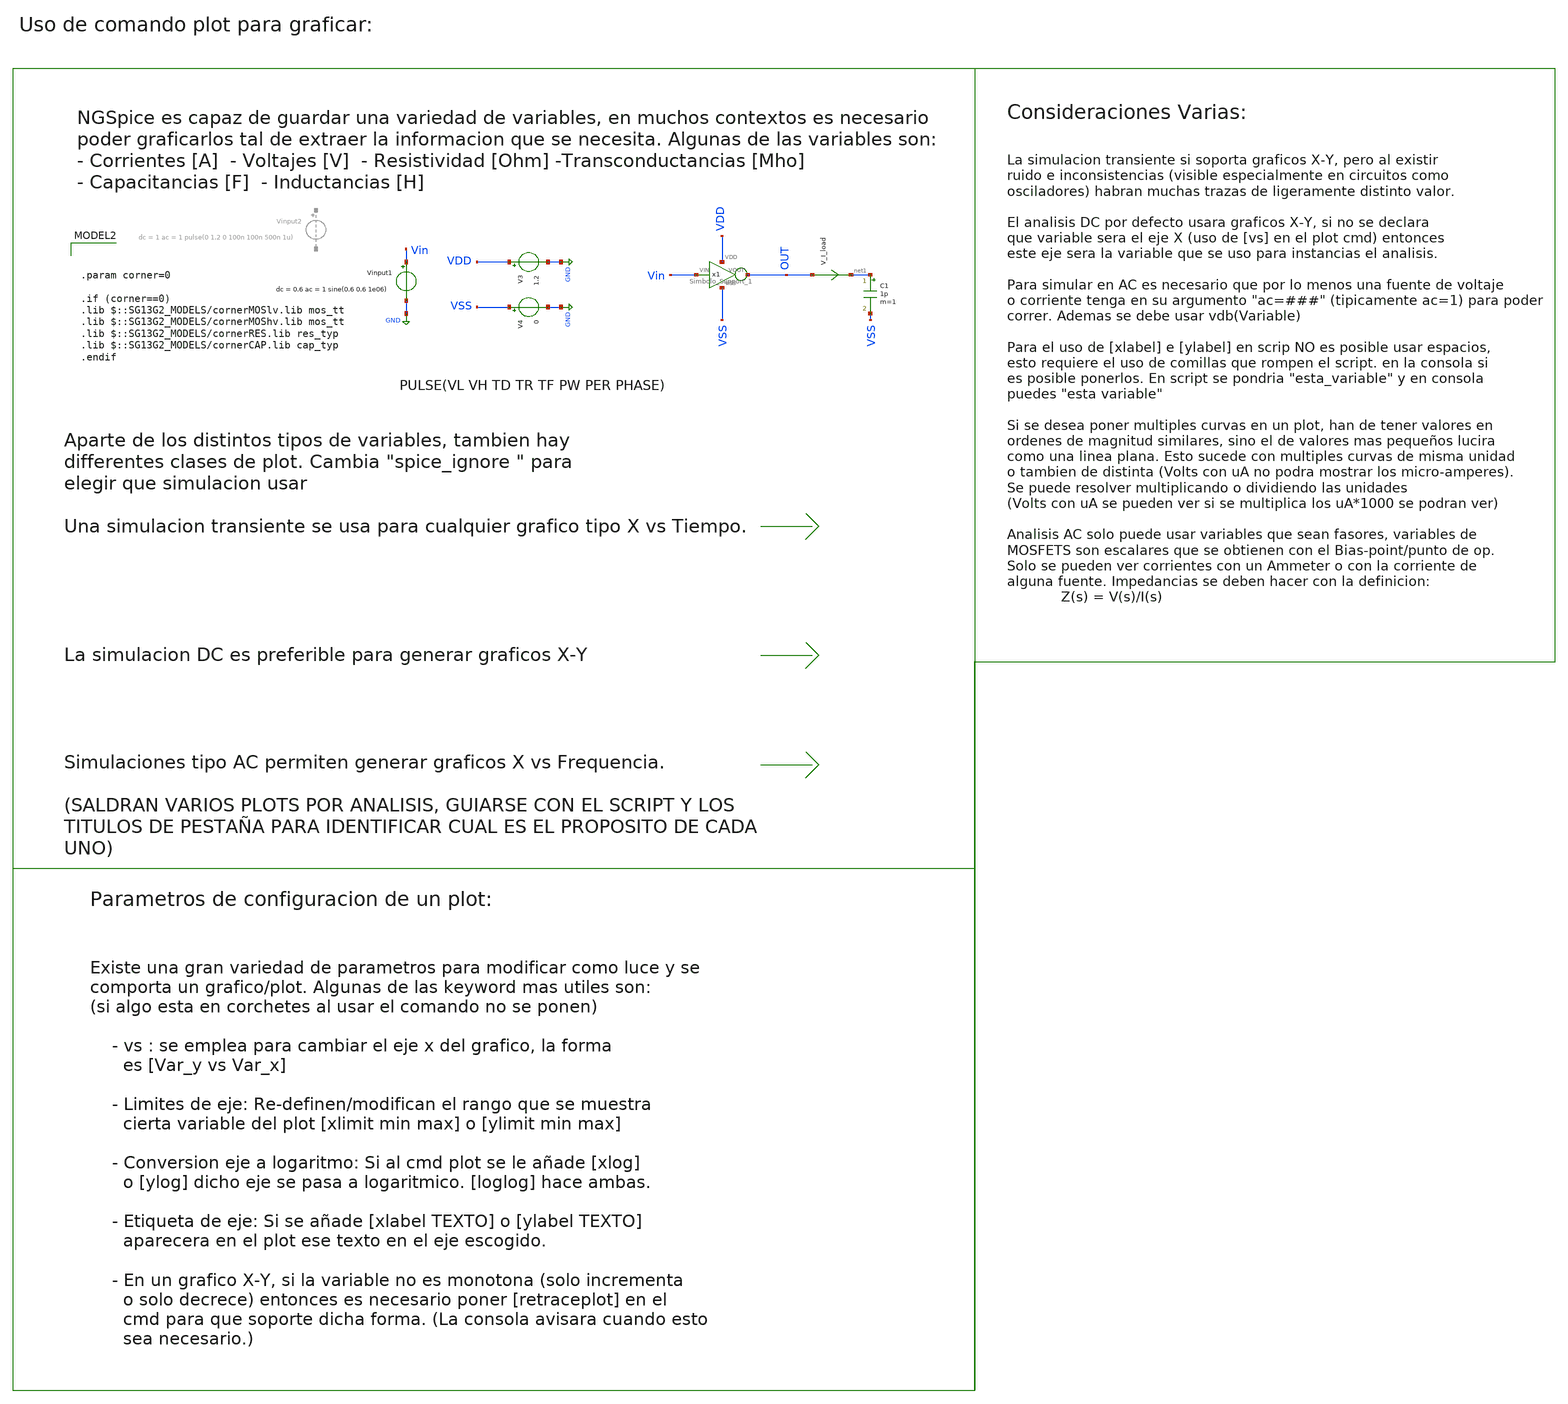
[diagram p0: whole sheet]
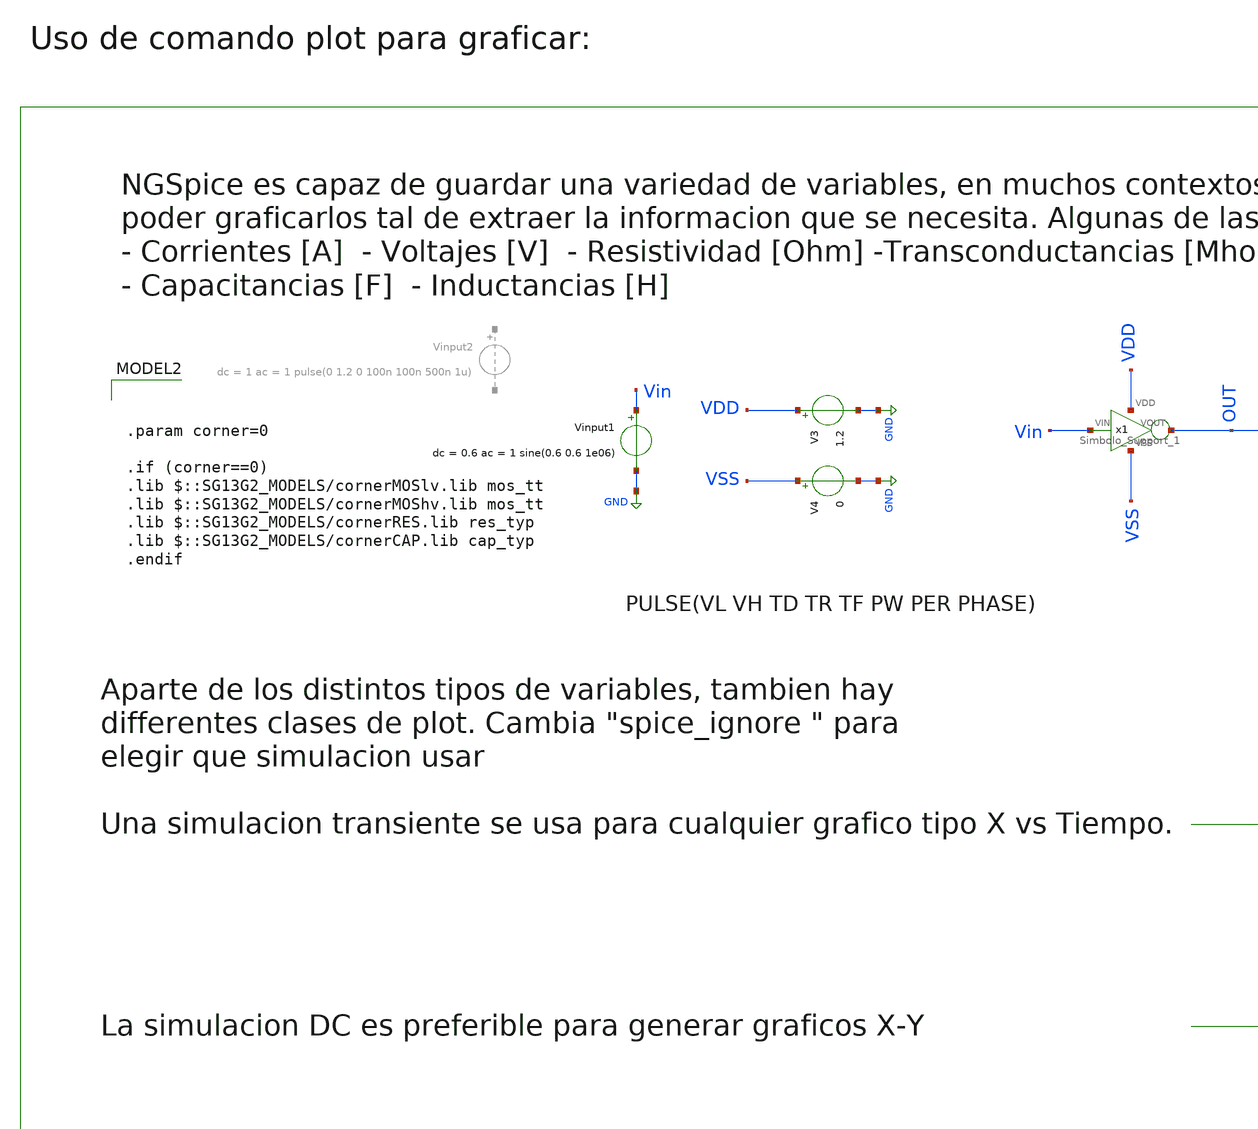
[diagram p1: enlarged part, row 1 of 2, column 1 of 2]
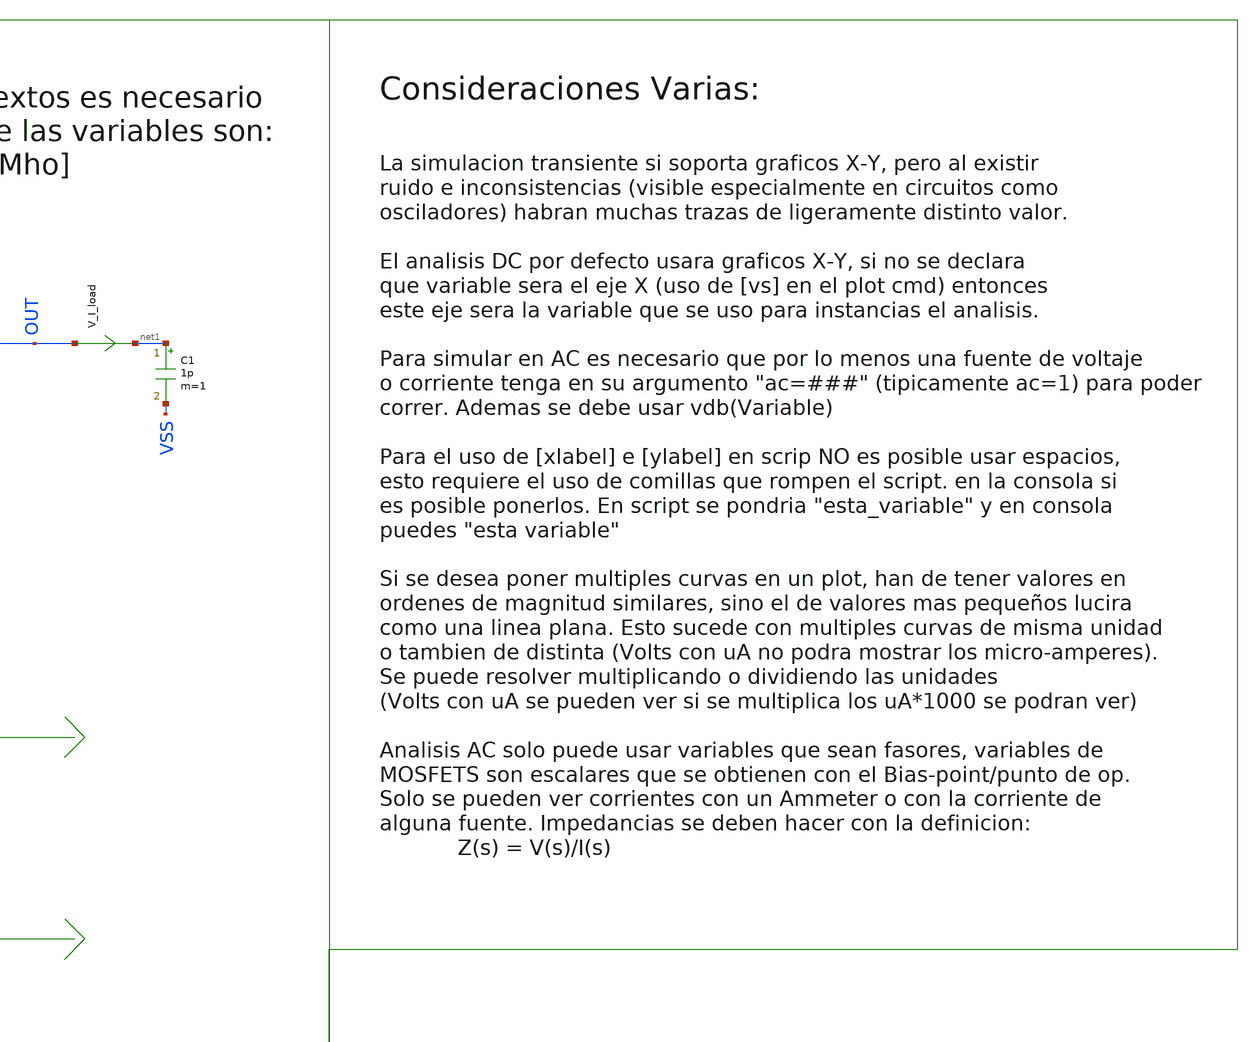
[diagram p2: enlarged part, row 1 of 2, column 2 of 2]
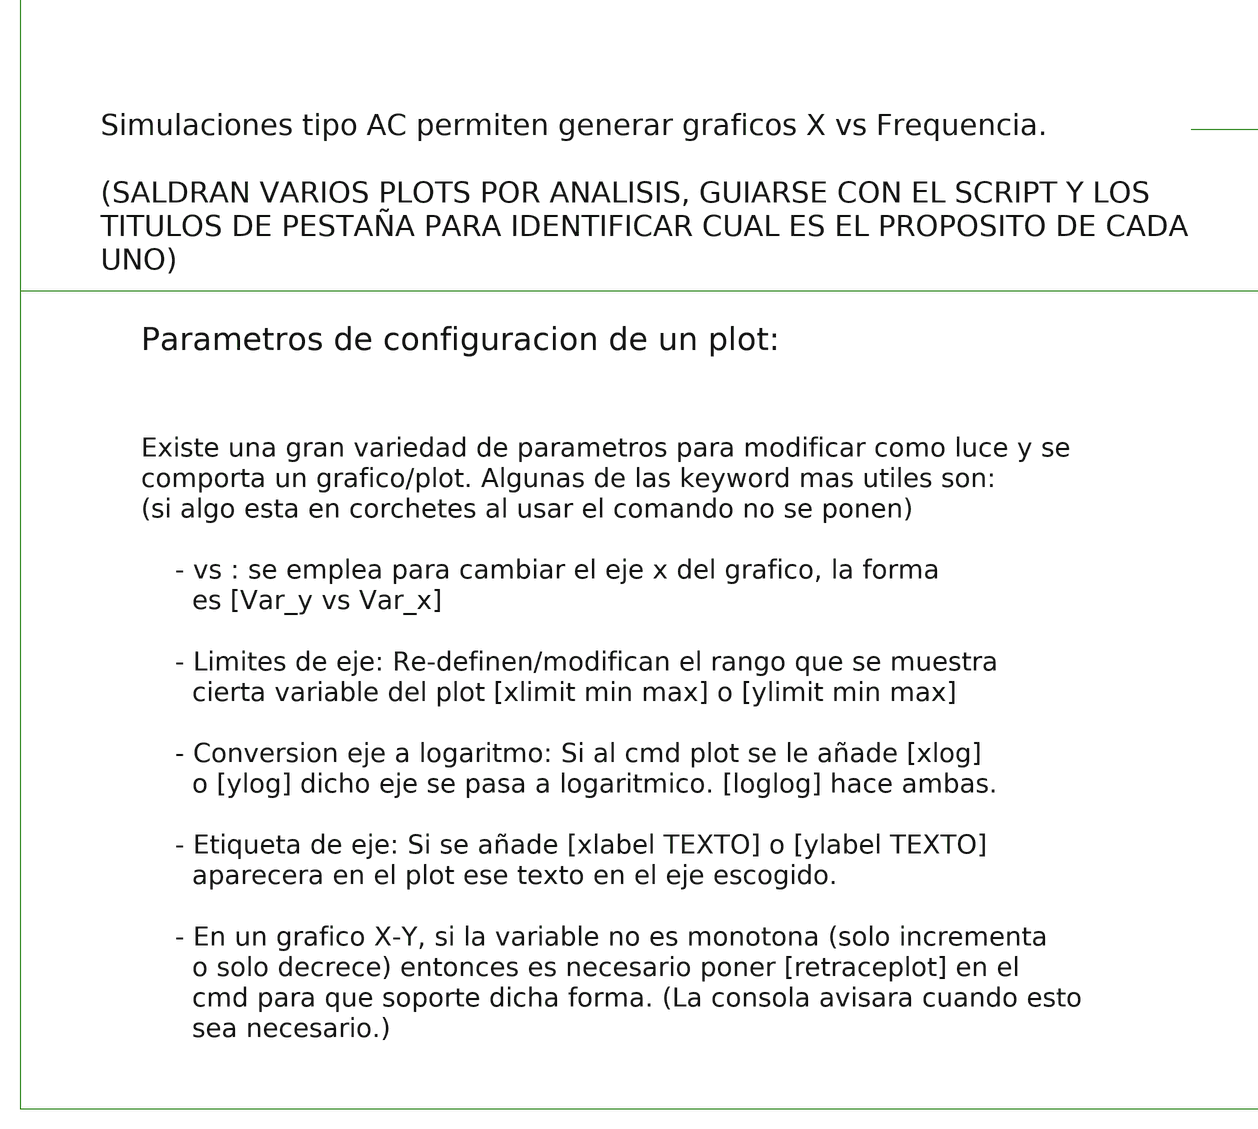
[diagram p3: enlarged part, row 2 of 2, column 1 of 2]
** sch_path: xschem/Manual_Instrucciones/Guia_plotting.sch
**.subckt Guia_plotting
V3 VDD GND 1.2
V4 VSS GND 0
Vinput1 Vin GND dc = 0.6 ac = 1 sine(0.6 0.6 1e06)
C1 net1 VSS 1p m=1
x1 VDD Vin OUT VSS Simbolo_Support_1
V_I_load OUT net1 0
.save i(v_i_load)
**** begin user architecture code


.param corner=0

.if (corner==0)
.lib $::SG13G2_MODELS/cornerMOSlv.lib mos_tt
.lib $::SG13G2_MODELS/cornerMOShv.lib mos_tt
.lib $::SG13G2_MODELS/cornerRES.lib res_typ
.lib $::SG13G2_MODELS/cornerCAP.lib cap_typ
.endif

**** end user architecture code
**.ends

* expanding   symbol:  ../Manual_Instrucciones/simbolos/Simbolo_Support_1.sym # of pins=4
** sym_path: ../Manual_Instrucciones/simbolos/Simbolo_Support_1.sym
** sch_path: ../Manual_Instrucciones/simbolos/Simbolo_Support_1.sch
.subckt Simbolo_Support_1 VDD VIN VOUT VSS
*.ipin VIN
*.iopin VDD
*.iopin VSS
*.opin VOUT
XM1 VOUT VIN VDD VDD sg13_lv_pmos w=2u l=0.13u ng=1 m=1 mm_ok=1
XM2 VOUT VIN VSS VSS sg13_lv_nmos w=1.0u l=0.13u ng=1 m=1 mm_ok=1
.ends

.GLOBAL GND
.end
